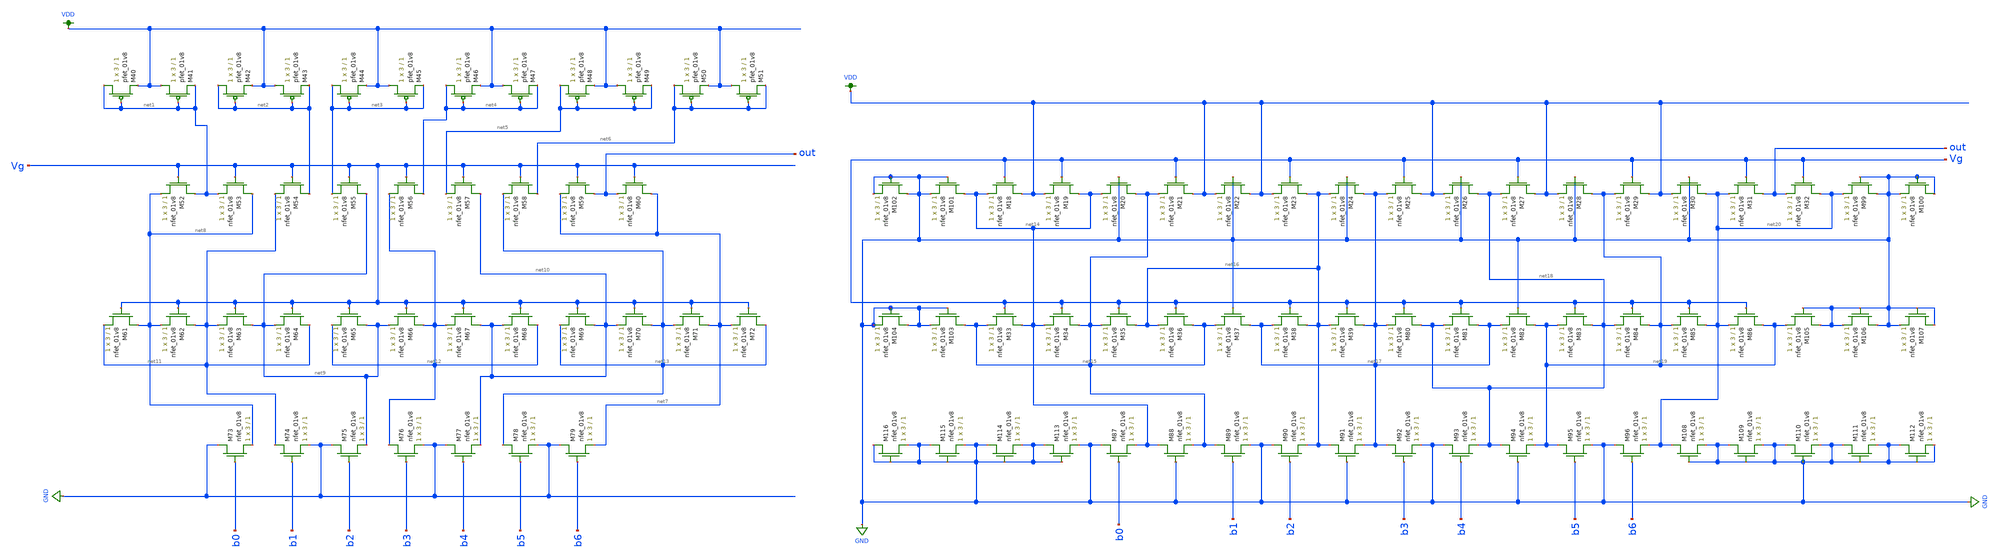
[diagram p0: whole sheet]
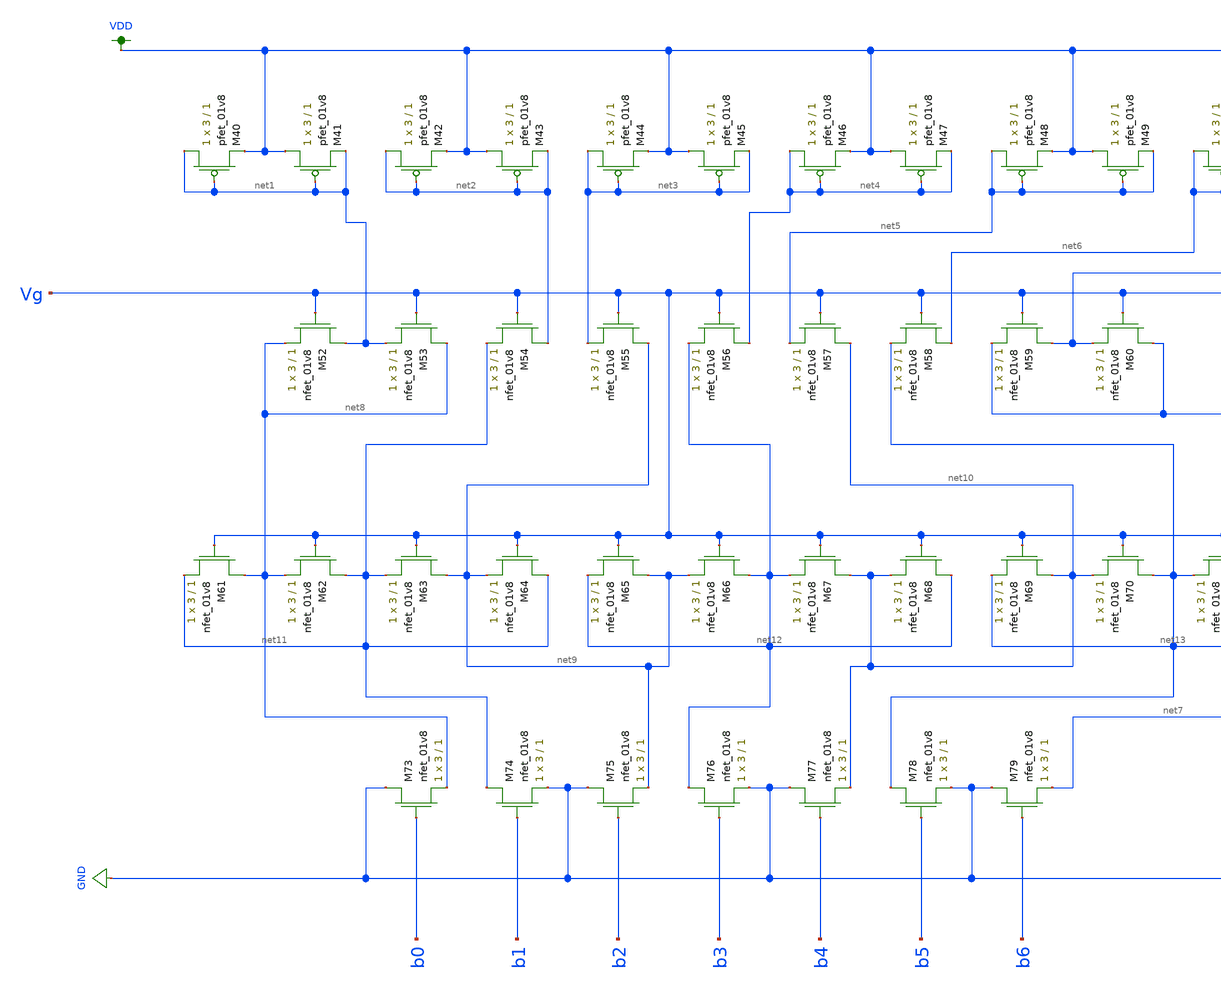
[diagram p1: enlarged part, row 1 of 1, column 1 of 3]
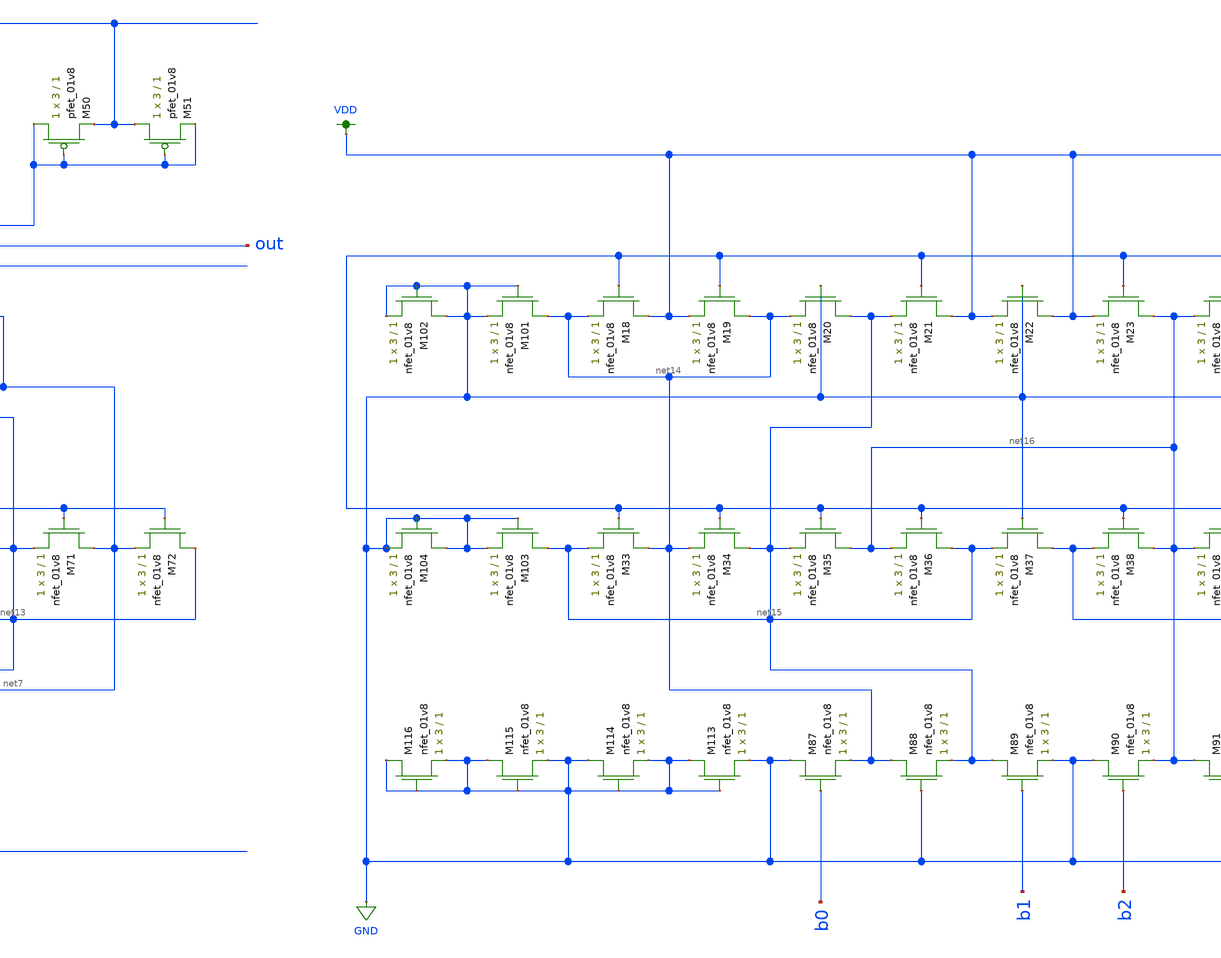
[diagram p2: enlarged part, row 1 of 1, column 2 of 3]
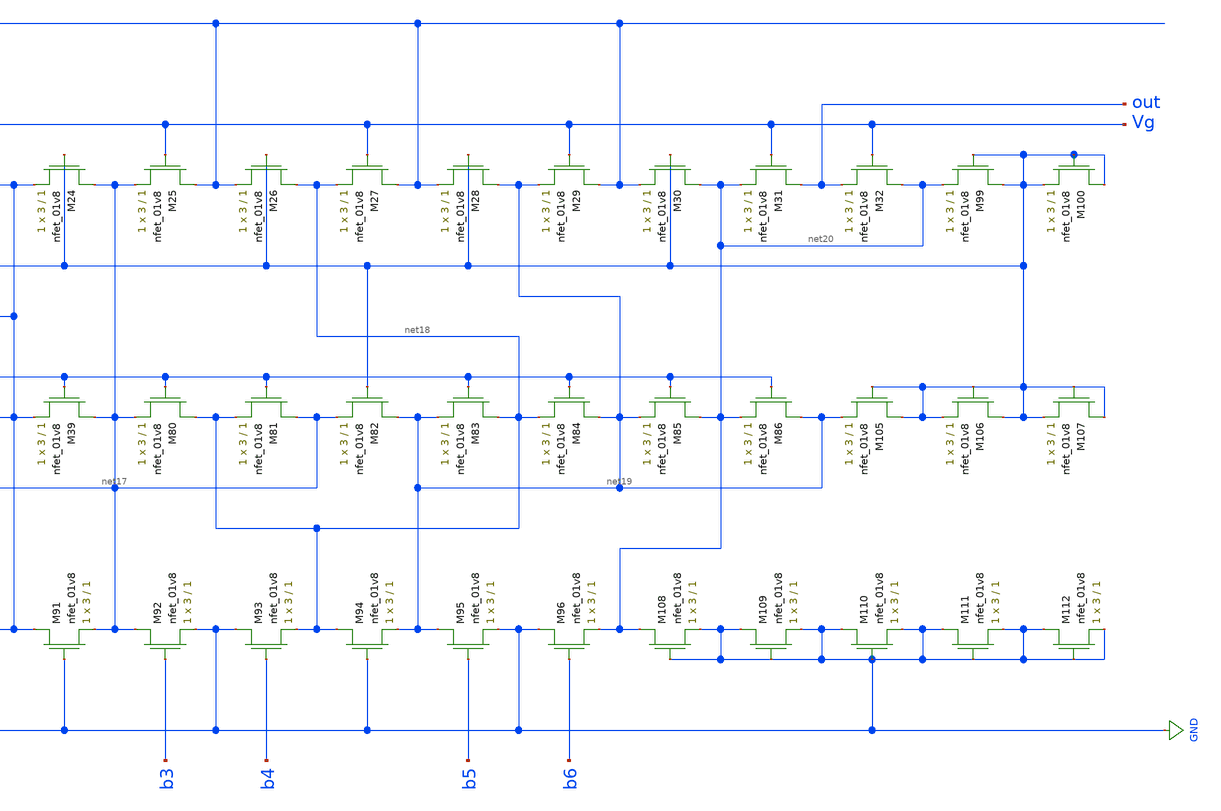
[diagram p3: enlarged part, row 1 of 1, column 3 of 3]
** sch_path: schematic/LDS/old/dac_7_bit_LDS_old.sch
**.subckt dac_7_bit_LDS_old
XM40 net1 net1 VDD VDD sky130_fd_pr__pfet_01v8 L=1 W=3 nf=1 ad='int((nf+1)/2) * W/nf * 0.29' as='int((nf+2)/2) * W/nf * 0.29'
+ pd='2*int((nf+1)/2) * (W/nf + 0.29)' ps='2*int((nf+2)/2) * (W/nf + 0.29)' nrd='0.29 / W' nrs='0.29 / W'
+ sa=0 sb=0 sd=0 mult=1 m=1
XM41 VDD net1 net1 VDD sky130_fd_pr__pfet_01v8 L=1 W=3 nf=1 ad='int((nf+1)/2) * W/nf * 0.29' as='int((nf+2)/2) * W/nf * 0.29'
+ pd='2*int((nf+1)/2) * (W/nf + 0.29)' ps='2*int((nf+2)/2) * (W/nf + 0.29)' nrd='0.29 / W' nrs='0.29 / W'
+ sa=0 sb=0 sd=0 mult=1 m=1
XM42 net2 net2 VDD VDD sky130_fd_pr__pfet_01v8 L=1 W=3 nf=1 ad='int((nf+1)/2) * W/nf * 0.29' as='int((nf+2)/2) * W/nf * 0.29'
+ pd='2*int((nf+1)/2) * (W/nf + 0.29)' ps='2*int((nf+2)/2) * (W/nf + 0.29)' nrd='0.29 / W' nrs='0.29 / W'
+ sa=0 sb=0 sd=0 mult=1 m=1
XM43 VDD net2 net2 VDD sky130_fd_pr__pfet_01v8 L=1 W=3 nf=1 ad='int((nf+1)/2) * W/nf * 0.29' as='int((nf+2)/2) * W/nf * 0.29'
+ pd='2*int((nf+1)/2) * (W/nf + 0.29)' ps='2*int((nf+2)/2) * (W/nf + 0.29)' nrd='0.29 / W' nrs='0.29 / W'
+ sa=0 sb=0 sd=0 mult=1 m=1
XM44 net3 net3 VDD VDD sky130_fd_pr__pfet_01v8 L=1 W=3 nf=1 ad='int((nf+1)/2) * W/nf * 0.29' as='int((nf+2)/2) * W/nf * 0.29'
+ pd='2*int((nf+1)/2) * (W/nf + 0.29)' ps='2*int((nf+2)/2) * (W/nf + 0.29)' nrd='0.29 / W' nrs='0.29 / W'
+ sa=0 sb=0 sd=0 mult=1 m=1
XM45 VDD net3 net3 VDD sky130_fd_pr__pfet_01v8 L=1 W=3 nf=1 ad='int((nf+1)/2) * W/nf * 0.29' as='int((nf+2)/2) * W/nf * 0.29'
+ pd='2*int((nf+1)/2) * (W/nf + 0.29)' ps='2*int((nf+2)/2) * (W/nf + 0.29)' nrd='0.29 / W' nrs='0.29 / W'
+ sa=0 sb=0 sd=0 mult=1 m=1
XM46 net4 net4 VDD VDD sky130_fd_pr__pfet_01v8 L=1 W=3 nf=1 ad='int((nf+1)/2) * W/nf * 0.29' as='int((nf+2)/2) * W/nf * 0.29'
+ pd='2*int((nf+1)/2) * (W/nf + 0.29)' ps='2*int((nf+2)/2) * (W/nf + 0.29)' nrd='0.29 / W' nrs='0.29 / W'
+ sa=0 sb=0 sd=0 mult=1 m=1
XM47 VDD net4 net4 VDD sky130_fd_pr__pfet_01v8 L=1 W=3 nf=1 ad='int((nf+1)/2) * W/nf * 0.29' as='int((nf+2)/2) * W/nf * 0.29'
+ pd='2*int((nf+1)/2) * (W/nf + 0.29)' ps='2*int((nf+2)/2) * (W/nf + 0.29)' nrd='0.29 / W' nrs='0.29 / W'
+ sa=0 sb=0 sd=0 mult=1 m=1
XM48 net5 net5 VDD VDD sky130_fd_pr__pfet_01v8 L=1 W=3 nf=1 ad='int((nf+1)/2) * W/nf * 0.29' as='int((nf+2)/2) * W/nf * 0.29'
+ pd='2*int((nf+1)/2) * (W/nf + 0.29)' ps='2*int((nf+2)/2) * (W/nf + 0.29)' nrd='0.29 / W' nrs='0.29 / W'
+ sa=0 sb=0 sd=0 mult=1 m=1
XM49 VDD net5 net5 VDD sky130_fd_pr__pfet_01v8 L=1 W=3 nf=1 ad='int((nf+1)/2) * W/nf * 0.29' as='int((nf+2)/2) * W/nf * 0.29'
+ pd='2*int((nf+1)/2) * (W/nf + 0.29)' ps='2*int((nf+2)/2) * (W/nf + 0.29)' nrd='0.29 / W' nrs='0.29 / W'
+ sa=0 sb=0 sd=0 mult=1 m=1
XM50 net6 net6 VDD VDD sky130_fd_pr__pfet_01v8 L=1 W=3 nf=1 ad='int((nf+1)/2) * W/nf * 0.29' as='int((nf+2)/2) * W/nf * 0.29'
+ pd='2*int((nf+1)/2) * (W/nf + 0.29)' ps='2*int((nf+2)/2) * (W/nf + 0.29)' nrd='0.29 / W' nrs='0.29 / W'
+ sa=0 sb=0 sd=0 mult=1 m=1
XM51 VDD net6 net6 VDD sky130_fd_pr__pfet_01v8 L=1 W=3 nf=1 ad='int((nf+1)/2) * W/nf * 0.29' as='int((nf+2)/2) * W/nf * 0.29'
+ pd='2*int((nf+1)/2) * (W/nf + 0.29)' ps='2*int((nf+2)/2) * (W/nf + 0.29)' nrd='0.29 / W' nrs='0.29 / W'
+ sa=0 sb=0 sd=0 mult=1 m=1
XM52 net1 Vg net8 GND sky130_fd_pr__nfet_01v8 L=1 W=3 nf=1 ad='int((nf+1)/2) * W/nf * 0.29' as='int((nf+2)/2) * W/nf * 0.29'
+ pd='2*int((nf+1)/2) * (W/nf + 0.29)' ps='2*int((nf+2)/2) * (W/nf + 0.29)' nrd='0.29 / W' nrs='0.29 / W'
+ sa=0 sb=0 sd=0 mult=1 m=1
XM53 net8 Vg net1 GND sky130_fd_pr__nfet_01v8 L=1 W=3 nf=1 ad='int((nf+1)/2) * W/nf * 0.29' as='int((nf+2)/2) * W/nf * 0.29'
+ pd='2*int((nf+1)/2) * (W/nf + 0.29)' ps='2*int((nf+2)/2) * (W/nf + 0.29)' nrd='0.29 / W' nrs='0.29 / W'
+ sa=0 sb=0 sd=0 mult=1 m=1
XM54 net2 Vg net11 GND sky130_fd_pr__nfet_01v8 L=1 W=3 nf=1 ad='int((nf+1)/2) * W/nf * 0.29' as='int((nf+2)/2) * W/nf * 0.29'
+ pd='2*int((nf+1)/2) * (W/nf + 0.29)' ps='2*int((nf+2)/2) * (W/nf + 0.29)' nrd='0.29 / W' nrs='0.29 / W'
+ sa=0 sb=0 sd=0 mult=1 m=1
XM55 net9 Vg net3 GND sky130_fd_pr__nfet_01v8 L=1 W=3 nf=1 ad='int((nf+1)/2) * W/nf * 0.29' as='int((nf+2)/2) * W/nf * 0.29'
+ pd='2*int((nf+1)/2) * (W/nf + 0.29)' ps='2*int((nf+2)/2) * (W/nf + 0.29)' nrd='0.29 / W' nrs='0.29 / W'
+ sa=0 sb=0 sd=0 mult=1 m=1
XM56 net4 Vg net12 GND sky130_fd_pr__nfet_01v8 L=1 W=3 nf=1 ad='int((nf+1)/2) * W/nf * 0.29' as='int((nf+2)/2) * W/nf * 0.29'
+ pd='2*int((nf+1)/2) * (W/nf + 0.29)' ps='2*int((nf+2)/2) * (W/nf + 0.29)' nrd='0.29 / W' nrs='0.29 / W'
+ sa=0 sb=0 sd=0 mult=1 m=1
XM57 net10 Vg net5 GND sky130_fd_pr__nfet_01v8 L=1 W=3 nf=1 ad='int((nf+1)/2) * W/nf * 0.29' as='int((nf+2)/2) * W/nf * 0.29'
+ pd='2*int((nf+1)/2) * (W/nf + 0.29)' ps='2*int((nf+2)/2) * (W/nf + 0.29)' nrd='0.29 / W' nrs='0.29 / W'
+ sa=0 sb=0 sd=0 mult=1 m=1
XM58 net6 Vg net13 GND sky130_fd_pr__nfet_01v8 L=1 W=3 nf=1 ad='int((nf+1)/2) * W/nf * 0.29' as='int((nf+2)/2) * W/nf * 0.29'
+ pd='2*int((nf+1)/2) * (W/nf + 0.29)' ps='2*int((nf+2)/2) * (W/nf + 0.29)' nrd='0.29 / W' nrs='0.29 / W'
+ sa=0 sb=0 sd=0 mult=1 m=1
XM59 out Vg net7 GND sky130_fd_pr__nfet_01v8 L=1 W=3 nf=1 ad='int((nf+1)/2) * W/nf * 0.29' as='int((nf+2)/2) * W/nf * 0.29'
+ pd='2*int((nf+1)/2) * (W/nf + 0.29)' ps='2*int((nf+2)/2) * (W/nf + 0.29)' nrd='0.29 / W' nrs='0.29 / W'
+ sa=0 sb=0 sd=0 mult=1 m=1
XM60 net7 Vg out GND sky130_fd_pr__nfet_01v8 L=1 W=3 nf=1 ad='int((nf+1)/2) * W/nf * 0.29' as='int((nf+2)/2) * W/nf * 0.29'
+ pd='2*int((nf+1)/2) * (W/nf + 0.29)' ps='2*int((nf+2)/2) * (W/nf + 0.29)' nrd='0.29 / W' nrs='0.29 / W'
+ sa=0 sb=0 sd=0 mult=1 m=1
XM61 net8 Vg net11 GND sky130_fd_pr__nfet_01v8 L=1 W=3 nf=1 ad='int((nf+1)/2) * W/nf * 0.29' as='int((nf+2)/2) * W/nf * 0.29'
+ pd='2*int((nf+1)/2) * (W/nf + 0.29)' ps='2*int((nf+2)/2) * (W/nf + 0.29)' nrd='0.29 / W' nrs='0.29 / W'
+ sa=0 sb=0 sd=0 mult=1 m=1
XM62 net11 Vg net8 GND sky130_fd_pr__nfet_01v8 L=1 W=3 nf=1 ad='int((nf+1)/2) * W/nf * 0.29' as='int((nf+2)/2) * W/nf * 0.29'
+ pd='2*int((nf+1)/2) * (W/nf + 0.29)' ps='2*int((nf+2)/2) * (W/nf + 0.29)' nrd='0.29 / W' nrs='0.29 / W'
+ sa=0 sb=0 sd=0 mult=1 m=1
XM63 net9 Vg net11 GND sky130_fd_pr__nfet_01v8 L=1 W=3 nf=1 ad='int((nf+1)/2) * W/nf * 0.29' as='int((nf+2)/2) * W/nf * 0.29'
+ pd='2*int((nf+1)/2) * (W/nf + 0.29)' ps='2*int((nf+2)/2) * (W/nf + 0.29)' nrd='0.29 / W' nrs='0.29 / W'
+ sa=0 sb=0 sd=0 mult=1 m=1
XM64 net11 Vg net9 GND sky130_fd_pr__nfet_01v8 L=1 W=3 nf=1 ad='int((nf+1)/2) * W/nf * 0.29' as='int((nf+2)/2) * W/nf * 0.29'
+ pd='2*int((nf+1)/2) * (W/nf + 0.29)' ps='2*int((nf+2)/2) * (W/nf + 0.29)' nrd='0.29 / W' nrs='0.29 / W'
+ sa=0 sb=0 sd=0 mult=1 m=1
XM65 net9 Vg net12 GND sky130_fd_pr__nfet_01v8 L=1 W=3 nf=1 ad='int((nf+1)/2) * W/nf * 0.29' as='int((nf+2)/2) * W/nf * 0.29'
+ pd='2*int((nf+1)/2) * (W/nf + 0.29)' ps='2*int((nf+2)/2) * (W/nf + 0.29)' nrd='0.29 / W' nrs='0.29 / W'
+ sa=0 sb=0 sd=0 mult=1 m=1
XM66 net12 Vg net9 GND sky130_fd_pr__nfet_01v8 L=1 W=3 nf=1 ad='int((nf+1)/2) * W/nf * 0.29' as='int((nf+2)/2) * W/nf * 0.29'
+ pd='2*int((nf+1)/2) * (W/nf + 0.29)' ps='2*int((nf+2)/2) * (W/nf + 0.29)' nrd='0.29 / W' nrs='0.29 / W'
+ sa=0 sb=0 sd=0 mult=1 m=1
XM67 net10 Vg net12 GND sky130_fd_pr__nfet_01v8 L=1 W=3 nf=1 ad='int((nf+1)/2) * W/nf * 0.29' as='int((nf+2)/2) * W/nf * 0.29'
+ pd='2*int((nf+1)/2) * (W/nf + 0.29)' ps='2*int((nf+2)/2) * (W/nf + 0.29)' nrd='0.29 / W' nrs='0.29 / W'
+ sa=0 sb=0 sd=0 mult=1 m=1
XM68 net12 Vg net10 GND sky130_fd_pr__nfet_01v8 L=1 W=3 nf=1 ad='int((nf+1)/2) * W/nf * 0.29' as='int((nf+2)/2) * W/nf * 0.29'
+ pd='2*int((nf+1)/2) * (W/nf + 0.29)' ps='2*int((nf+2)/2) * (W/nf + 0.29)' nrd='0.29 / W' nrs='0.29 / W'
+ sa=0 sb=0 sd=0 mult=1 m=1
XM69 net10 Vg net13 GND sky130_fd_pr__nfet_01v8 L=1 W=3 nf=1 ad='int((nf+1)/2) * W/nf * 0.29' as='int((nf+2)/2) * W/nf * 0.29'
+ pd='2*int((nf+1)/2) * (W/nf + 0.29)' ps='2*int((nf+2)/2) * (W/nf + 0.29)' nrd='0.29 / W' nrs='0.29 / W'
+ sa=0 sb=0 sd=0 mult=1 m=1
XM70 net13 Vg net10 GND sky130_fd_pr__nfet_01v8 L=1 W=3 nf=1 ad='int((nf+1)/2) * W/nf * 0.29' as='int((nf+2)/2) * W/nf * 0.29'
+ pd='2*int((nf+1)/2) * (W/nf + 0.29)' ps='2*int((nf+2)/2) * (W/nf + 0.29)' nrd='0.29 / W' nrs='0.29 / W'
+ sa=0 sb=0 sd=0 mult=1 m=1
XM71 net7 Vg net13 GND sky130_fd_pr__nfet_01v8 L=1 W=3 nf=1 ad='int((nf+1)/2) * W/nf * 0.29' as='int((nf+2)/2) * W/nf * 0.29'
+ pd='2*int((nf+1)/2) * (W/nf + 0.29)' ps='2*int((nf+2)/2) * (W/nf + 0.29)' nrd='0.29 / W' nrs='0.29 / W'
+ sa=0 sb=0 sd=0 mult=1 m=1
XM72 net13 Vg net7 GND sky130_fd_pr__nfet_01v8 L=1 W=3 nf=1 ad='int((nf+1)/2) * W/nf * 0.29' as='int((nf+2)/2) * W/nf * 0.29'
+ pd='2*int((nf+1)/2) * (W/nf + 0.29)' ps='2*int((nf+2)/2) * (W/nf + 0.29)' nrd='0.29 / W' nrs='0.29 / W'
+ sa=0 sb=0 sd=0 mult=1 m=1
XM73 GND b0 net8 GND sky130_fd_pr__nfet_01v8 L=1 W=3 nf=1 ad='int((nf+1)/2) * W/nf * 0.29' as='int((nf+2)/2) * W/nf * 0.29'
+ pd='2*int((nf+1)/2) * (W/nf + 0.29)' ps='2*int((nf+2)/2) * (W/nf + 0.29)' nrd='0.29 / W' nrs='0.29 / W'
+ sa=0 sb=0 sd=0 mult=1 m=1
XM74 net11 b1 GND GND sky130_fd_pr__nfet_01v8 L=1 W=3 nf=1 ad='int((nf+1)/2) * W/nf * 0.29' as='int((nf+2)/2) * W/nf * 0.29'
+ pd='2*int((nf+1)/2) * (W/nf + 0.29)' ps='2*int((nf+2)/2) * (W/nf + 0.29)' nrd='0.29 / W' nrs='0.29 / W'
+ sa=0 sb=0 sd=0 mult=1 m=1
XM75 GND b2 net9 GND sky130_fd_pr__nfet_01v8 L=1 W=3 nf=1 ad='int((nf+1)/2) * W/nf * 0.29' as='int((nf+2)/2) * W/nf * 0.29'
+ pd='2*int((nf+1)/2) * (W/nf + 0.29)' ps='2*int((nf+2)/2) * (W/nf + 0.29)' nrd='0.29 / W' nrs='0.29 / W'
+ sa=0 sb=0 sd=0 mult=1 m=1
XM76 net12 b3 GND GND sky130_fd_pr__nfet_01v8 L=1 W=3 nf=1 ad='int((nf+1)/2) * W/nf * 0.29' as='int((nf+2)/2) * W/nf * 0.29'
+ pd='2*int((nf+1)/2) * (W/nf + 0.29)' ps='2*int((nf+2)/2) * (W/nf + 0.29)' nrd='0.29 / W' nrs='0.29 / W'
+ sa=0 sb=0 sd=0 mult=1 m=1
XM77 GND b4 net10 GND sky130_fd_pr__nfet_01v8 L=1 W=3 nf=1 ad='int((nf+1)/2) * W/nf * 0.29' as='int((nf+2)/2) * W/nf * 0.29'
+ pd='2*int((nf+1)/2) * (W/nf + 0.29)' ps='2*int((nf+2)/2) * (W/nf + 0.29)' nrd='0.29 / W' nrs='0.29 / W'
+ sa=0 sb=0 sd=0 mult=1 m=1
XM78 net13 b5 GND GND sky130_fd_pr__nfet_01v8 L=1 W=3 nf=1 ad='int((nf+1)/2) * W/nf * 0.29' as='int((nf+2)/2) * W/nf * 0.29'
+ pd='2*int((nf+1)/2) * (W/nf + 0.29)' ps='2*int((nf+2)/2) * (W/nf + 0.29)' nrd='0.29 / W' nrs='0.29 / W'
+ sa=0 sb=0 sd=0 mult=1 m=1
XM79 GND b6 net7 GND sky130_fd_pr__nfet_01v8 L=1 W=3 nf=1 ad='int((nf+1)/2) * W/nf * 0.29' as='int((nf+2)/2) * W/nf * 0.29'
+ pd='2*int((nf+1)/2) * (W/nf + 0.29)' ps='2*int((nf+2)/2) * (W/nf + 0.29)' nrd='0.29 / W' nrs='0.29 / W'
+ sa=0 sb=0 sd=0 mult=1 m=1
XM18 VDD Vg net14 GND sky130_fd_pr__nfet_01v8 L=1 W=3 nf=1 ad='int((nf+1)/2) * W/nf * 0.29' as='int((nf+2)/2) * W/nf * 0.29'
+ pd='2*int((nf+1)/2) * (W/nf + 0.29)' ps='2*int((nf+2)/2) * (W/nf + 0.29)' nrd='0.29 / W' nrs='0.29 / W'
+ sa=0 sb=0 sd=0 mult=1 m=1
XM19 net14 Vg VDD GND sky130_fd_pr__nfet_01v8 L=1 W=3 nf=1 ad='int((nf+1)/2) * W/nf * 0.29' as='int((nf+2)/2) * W/nf * 0.29'
+ pd='2*int((nf+1)/2) * (W/nf + 0.29)' ps='2*int((nf+2)/2) * (W/nf + 0.29)' nrd='0.29 / W' nrs='0.29 / W'
+ sa=0 sb=0 sd=0 mult=1 m=1
XM20 net15 GND net14 GND sky130_fd_pr__nfet_01v8 L=1 W=3 nf=1 ad='int((nf+1)/2) * W/nf * 0.29' as='int((nf+2)/2) * W/nf * 0.29'
+ pd='2*int((nf+1)/2) * (W/nf + 0.29)' ps='2*int((nf+2)/2) * (W/nf + 0.29)' nrd='0.29 / W' nrs='0.29 / W'
+ sa=0 sb=0 sd=0 mult=1 m=1
XM21 VDD Vg net15 GND sky130_fd_pr__nfet_01v8 L=1 W=3 nf=1 ad='int((nf+1)/2) * W/nf * 0.29' as='int((nf+2)/2) * W/nf * 0.29'
+ pd='2*int((nf+1)/2) * (W/nf + 0.29)' ps='2*int((nf+2)/2) * (W/nf + 0.29)' nrd='0.29 / W' nrs='0.29 / W'
+ sa=0 sb=0 sd=0 mult=1 m=1
XM22 VDD GND VDD GND sky130_fd_pr__nfet_01v8 L=1 W=3 nf=1 ad='int((nf+1)/2) * W/nf * 0.29' as='int((nf+2)/2) * W/nf * 0.29'
+ pd='2*int((nf+1)/2) * (W/nf + 0.29)' ps='2*int((nf+2)/2) * (W/nf + 0.29)' nrd='0.29 / W' nrs='0.29 / W'
+ sa=0 sb=0 sd=0 mult=1 m=1
XM23 net16 Vg VDD GND sky130_fd_pr__nfet_01v8 L=1 W=3 nf=1 ad='int((nf+1)/2) * W/nf * 0.29' as='int((nf+2)/2) * W/nf * 0.29'
+ pd='2*int((nf+1)/2) * (W/nf + 0.29)' ps='2*int((nf+2)/2) * (W/nf + 0.29)' nrd='0.29 / W' nrs='0.29 / W'
+ sa=0 sb=0 sd=0 mult=1 m=1
XM24 net17 GND net16 GND sky130_fd_pr__nfet_01v8 L=1 W=3 nf=1 ad='int((nf+1)/2) * W/nf * 0.29' as='int((nf+2)/2) * W/nf * 0.29'
+ pd='2*int((nf+1)/2) * (W/nf + 0.29)' ps='2*int((nf+2)/2) * (W/nf + 0.29)' nrd='0.29 / W' nrs='0.29 / W'
+ sa=0 sb=0 sd=0 mult=1 m=1
XM25 VDD Vg net17 GND sky130_fd_pr__nfet_01v8 L=1 W=3 nf=1 ad='int((nf+1)/2) * W/nf * 0.29' as='int((nf+2)/2) * W/nf * 0.29'
+ pd='2*int((nf+1)/2) * (W/nf + 0.29)' ps='2*int((nf+2)/2) * (W/nf + 0.29)' nrd='0.29 / W' nrs='0.29 / W'
+ sa=0 sb=0 sd=0 mult=1 m=1
XM26 net18 GND VDD GND sky130_fd_pr__nfet_01v8 L=1 W=3 nf=1 ad='int((nf+1)/2) * W/nf * 0.29' as='int((nf+2)/2) * W/nf * 0.29'
+ pd='2*int((nf+1)/2) * (W/nf + 0.29)' ps='2*int((nf+2)/2) * (W/nf + 0.29)' nrd='0.29 / W' nrs='0.29 / W'
+ sa=0 sb=0 sd=0 mult=1 m=1
XM27 VDD Vg net18 GND sky130_fd_pr__nfet_01v8 L=1 W=3 nf=1 ad='int((nf+1)/2) * W/nf * 0.29' as='int((nf+2)/2) * W/nf * 0.29'
+ pd='2*int((nf+1)/2) * (W/nf + 0.29)' ps='2*int((nf+2)/2) * (W/nf + 0.29)' nrd='0.29 / W' nrs='0.29 / W'
+ sa=0 sb=0 sd=0 mult=1 m=1
XM28 net19 GND VDD GND sky130_fd_pr__nfet_01v8 L=1 W=3 nf=1 ad='int((nf+1)/2) * W/nf * 0.29' as='int((nf+2)/2) * W/nf * 0.29'
+ pd='2*int((nf+1)/2) * (W/nf + 0.29)' ps='2*int((nf+2)/2) * (W/nf + 0.29)' nrd='0.29 / W' nrs='0.29 / W'
+ sa=0 sb=0 sd=0 mult=1 m=1
XM29 VDD Vg net19 GND sky130_fd_pr__nfet_01v8 L=1 W=3 nf=1 ad='int((nf+1)/2) * W/nf * 0.29' as='int((nf+2)/2) * W/nf * 0.29'
+ pd='2*int((nf+1)/2) * (W/nf + 0.29)' ps='2*int((nf+2)/2) * (W/nf + 0.29)' nrd='0.29 / W' nrs='0.29 / W'
+ sa=0 sb=0 sd=0 mult=1 m=1
XM30 net20 GND VDD GND sky130_fd_pr__nfet_01v8 L=1 W=3 nf=1 ad='int((nf+1)/2) * W/nf * 0.29' as='int((nf+2)/2) * W/nf * 0.29'
+ pd='2*int((nf+1)/2) * (W/nf + 0.29)' ps='2*int((nf+2)/2) * (W/nf + 0.29)' nrd='0.29 / W' nrs='0.29 / W'
+ sa=0 sb=0 sd=0 mult=1 m=1
XM31 out Vg net20 GND sky130_fd_pr__nfet_01v8 L=1 W=3 nf=1 ad='int((nf+1)/2) * W/nf * 0.29' as='int((nf+2)/2) * W/nf * 0.29'
+ pd='2*int((nf+1)/2) * (W/nf + 0.29)' ps='2*int((nf+2)/2) * (W/nf + 0.29)' nrd='0.29 / W' nrs='0.29 / W'
+ sa=0 sb=0 sd=0 mult=1 m=1
XM32 net20 Vg out GND sky130_fd_pr__nfet_01v8 L=1 W=3 nf=1 ad='int((nf+1)/2) * W/nf * 0.29' as='int((nf+2)/2) * W/nf * 0.29'
+ pd='2*int((nf+1)/2) * (W/nf + 0.29)' ps='2*int((nf+2)/2) * (W/nf + 0.29)' nrd='0.29 / W' nrs='0.29 / W'
+ sa=0 sb=0 sd=0 mult=1 m=1
XM33 net14 Vg net15 GND sky130_fd_pr__nfet_01v8 L=1 W=3 nf=1 ad='int((nf+1)/2) * W/nf * 0.29' as='int((nf+2)/2) * W/nf * 0.29'
+ pd='2*int((nf+1)/2) * (W/nf + 0.29)' ps='2*int((nf+2)/2) * (W/nf + 0.29)' nrd='0.29 / W' nrs='0.29 / W'
+ sa=0 sb=0 sd=0 mult=1 m=1
XM34 net15 Vg net14 GND sky130_fd_pr__nfet_01v8 L=1 W=3 nf=1 ad='int((nf+1)/2) * W/nf * 0.29' as='int((nf+2)/2) * W/nf * 0.29'
+ pd='2*int((nf+1)/2) * (W/nf + 0.29)' ps='2*int((nf+2)/2) * (W/nf + 0.29)' nrd='0.29 / W' nrs='0.29 / W'
+ sa=0 sb=0 sd=0 mult=1 m=1
XM35 net16 Vg net15 GND sky130_fd_pr__nfet_01v8 L=1 W=3 nf=1 ad='int((nf+1)/2) * W/nf * 0.29' as='int((nf+2)/2) * W/nf * 0.29'
+ pd='2*int((nf+1)/2) * (W/nf + 0.29)' ps='2*int((nf+2)/2) * (W/nf + 0.29)' nrd='0.29 / W' nrs='0.29 / W'
+ sa=0 sb=0 sd=0 mult=1 m=1
XM36 net15 Vg net16 GND sky130_fd_pr__nfet_01v8 L=1 W=3 nf=1 ad='int((nf+1)/2) * W/nf * 0.29' as='int((nf+2)/2) * W/nf * 0.29'
+ pd='2*int((nf+1)/2) * (W/nf + 0.29)' ps='2*int((nf+2)/2) * (W/nf + 0.29)' nrd='0.29 / W' nrs='0.29 / W'
+ sa=0 sb=0 sd=0 mult=1 m=1
XM37 net17 GND net15 GND sky130_fd_pr__nfet_01v8 L=1 W=3 nf=1 ad='int((nf+1)/2) * W/nf * 0.29' as='int((nf+2)/2) * W/nf * 0.29'
+ pd='2*int((nf+1)/2) * (W/nf + 0.29)' ps='2*int((nf+2)/2) * (W/nf + 0.29)' nrd='0.29 / W' nrs='0.29 / W'
+ sa=0 sb=0 sd=0 mult=1 m=1
XM38 net16 Vg net17 GND sky130_fd_pr__nfet_01v8 L=1 W=3 nf=1 ad='int((nf+1)/2) * W/nf * 0.29' as='int((nf+2)/2) * W/nf * 0.29'
+ pd='2*int((nf+1)/2) * (W/nf + 0.29)' ps='2*int((nf+2)/2) * (W/nf + 0.29)' nrd='0.29 / W' nrs='0.29 / W'
+ sa=0 sb=0 sd=0 mult=1 m=1
XM39 net17 Vg net16 GND sky130_fd_pr__nfet_01v8 L=1 W=3 nf=1 ad='int((nf+1)/2) * W/nf * 0.29' as='int((nf+2)/2) * W/nf * 0.29'
+ pd='2*int((nf+1)/2) * (W/nf + 0.29)' ps='2*int((nf+2)/2) * (W/nf + 0.29)' nrd='0.29 / W' nrs='0.29 / W'
+ sa=0 sb=0 sd=0 mult=1 m=1
XM80 net18 Vg net17 GND sky130_fd_pr__nfet_01v8 L=1 W=3 nf=1 ad='int((nf+1)/2) * W/nf * 0.29' as='int((nf+2)/2) * W/nf * 0.29'
+ pd='2*int((nf+1)/2) * (W/nf + 0.29)' ps='2*int((nf+2)/2) * (W/nf + 0.29)' nrd='0.29 / W' nrs='0.29 / W'
+ sa=0 sb=0 sd=0 mult=1 m=1
XM81 net17 Vg net18 GND sky130_fd_pr__nfet_01v8 L=1 W=3 nf=1 ad='int((nf+1)/2) * W/nf * 0.29' as='int((nf+2)/2) * W/nf * 0.29'
+ pd='2*int((nf+1)/2) * (W/nf + 0.29)' ps='2*int((nf+2)/2) * (W/nf + 0.29)' nrd='0.29 / W' nrs='0.29 / W'
+ sa=0 sb=0 sd=0 mult=1 m=1
XM82 net19 GND net17 GND sky130_fd_pr__nfet_01v8 L=1 W=3 nf=1 ad='int((nf+1)/2) * W/nf * 0.29' as='int((nf+2)/2) * W/nf * 0.29'
+ pd='2*int((nf+1)/2) * (W/nf + 0.29)' ps='2*int((nf+2)/2) * (W/nf + 0.29)' nrd='0.29 / W' nrs='0.29 / W'
+ sa=0 sb=0 sd=0 mult=1 m=1
XM83 net18 Vg net19 GND sky130_fd_pr__nfet_01v8 L=1 W=3 nf=1 ad='int((nf+1)/2) * W/nf * 0.29' as='int((nf+2)/2) * W/nf * 0.29'
+ pd='2*int((nf+1)/2) * (W/nf + 0.29)' ps='2*int((nf+2)/2) * (W/nf + 0.29)' nrd='0.29 / W' nrs='0.29 / W'
+ sa=0 sb=0 sd=0 mult=1 m=1
XM84 net19 Vg net18 GND sky130_fd_pr__nfet_01v8 L=1 W=3 nf=1 ad='int((nf+1)/2) * W/nf * 0.29' as='int((nf+2)/2) * W/nf * 0.29'
+ pd='2*int((nf+1)/2) * (W/nf + 0.29)' ps='2*int((nf+2)/2) * (W/nf + 0.29)' nrd='0.29 / W' nrs='0.29 / W'
+ sa=0 sb=0 sd=0 mult=1 m=1
XM85 net20 Vg net19 GND sky130_fd_pr__nfet_01v8 L=1 W=3 nf=1 ad='int((nf+1)/2) * W/nf * 0.29' as='int((nf+2)/2) * W/nf * 0.29'
+ pd='2*int((nf+1)/2) * (W/nf + 0.29)' ps='2*int((nf+2)/2) * (W/nf + 0.29)' nrd='0.29 / W' nrs='0.29 / W'
+ sa=0 sb=0 sd=0 mult=1 m=1
XM86 net19 Vg net20 GND sky130_fd_pr__nfet_01v8 L=1 W=3 nf=1 ad='int((nf+1)/2) * W/nf * 0.29' as='int((nf+2)/2) * W/nf * 0.29'
+ pd='2*int((nf+1)/2) * (W/nf + 0.29)' ps='2*int((nf+2)/2) * (W/nf + 0.29)' nrd='0.29 / W' nrs='0.29 / W'
+ sa=0 sb=0 sd=0 mult=1 m=1
XM87 GND b0 net14 GND sky130_fd_pr__nfet_01v8 L=1 W=3 nf=1 ad='int((nf+1)/2) * W/nf * 0.29' as='int((nf+2)/2) * W/nf * 0.29'
+ pd='2*int((nf+1)/2) * (W/nf + 0.29)' ps='2*int((nf+2)/2) * (W/nf + 0.29)' nrd='0.29 / W' nrs='0.29 / W'
+ sa=0 sb=0 sd=0 mult=1 m=1
XM88 net14 GND net15 GND sky130_fd_pr__nfet_01v8 L=1 W=3 nf=1 ad='int((nf+1)/2) * W/nf * 0.29' as='int((nf+2)/2) * W/nf * 0.29'
+ pd='2*int((nf+1)/2) * (W/nf + 0.29)' ps='2*int((nf+2)/2) * (W/nf + 0.29)' nrd='0.29 / W' nrs='0.29 / W'
+ sa=0 sb=0 sd=0 mult=1 m=1
XM89 net15 b1 GND GND sky130_fd_pr__nfet_01v8 L=1 W=3 nf=1 ad='int((nf+1)/2) * W/nf * 0.29' as='int((nf+2)/2) * W/nf * 0.29'
+ pd='2*int((nf+1)/2) * (W/nf + 0.29)' ps='2*int((nf+2)/2) * (W/nf + 0.29)' nrd='0.29 / W' nrs='0.29 / W'
+ sa=0 sb=0 sd=0 mult=1 m=1
XM90 GND b2 net16 GND sky130_fd_pr__nfet_01v8 L=1 W=3 nf=1 ad='int((nf+1)/2) * W/nf * 0.29' as='int((nf+2)/2) * W/nf * 0.29'
+ pd='2*int((nf+1)/2) * (W/nf + 0.29)' ps='2*int((nf+2)/2) * (W/nf + 0.29)' nrd='0.29 / W' nrs='0.29 / W'
+ sa=0 sb=0 sd=0 mult=1 m=1
XM91 net16 GND net17 GND sky130_fd_pr__nfet_01v8 L=1 W=3 nf=1 ad='int((nf+1)/2) * W/nf * 0.29' as='int((nf+2)/2) * W/nf * 0.29'
+ pd='2*int((nf+1)/2) * (W/nf + 0.29)' ps='2*int((nf+2)/2) * (W/nf + 0.29)' nrd='0.29 / W' nrs='0.29 / W'
+ sa=0 sb=0 sd=0 mult=1 m=1
XM92 net17 b3 GND GND sky130_fd_pr__nfet_01v8 L=1 W=3 nf=1 ad='int((nf+1)/2) * W/nf * 0.29' as='int((nf+2)/2) * W/nf * 0.29'
+ pd='2*int((nf+1)/2) * (W/nf + 0.29)' ps='2*int((nf+2)/2) * (W/nf + 0.29)' nrd='0.29 / W' nrs='0.29 / W'
+ sa=0 sb=0 sd=0 mult=1 m=1
XM93 GND b4 net18 GND sky130_fd_pr__nfet_01v8 L=1 W=3 nf=1 ad='int((nf+1)/2) * W/nf * 0.29' as='int((nf+2)/2) * W/nf * 0.29'
+ pd='2*int((nf+1)/2) * (W/nf + 0.29)' ps='2*int((nf+2)/2) * (W/nf + 0.29)' nrd='0.29 / W' nrs='0.29 / W'
+ sa=0 sb=0 sd=0 mult=1 m=1
XM94 net18 GND net19 GND sky130_fd_pr__nfet_01v8 L=1 W=3 nf=1 ad='int((nf+1)/2) * W/nf * 0.29' as='int((nf+2)/2) * W/nf * 0.29'
+ pd='2*int((nf+1)/2) * (W/nf + 0.29)' ps='2*int((nf+2)/2) * (W/nf + 0.29)' nrd='0.29 / W' nrs='0.29 / W'
+ sa=0 sb=0 sd=0 mult=1 m=1
XM95 net19 b5 GND GND sky130_fd_pr__nfet_01v8 L=1 W=3 nf=1 ad='int((nf+1)/2) * W/nf * 0.29' as='int((nf+2)/2) * W/nf * 0.29'
+ pd='2*int((nf+1)/2) * (W/nf + 0.29)' ps='2*int((nf+2)/2) * (W/nf + 0.29)' nrd='0.29 / W' nrs='0.29 / W'
+ sa=0 sb=0 sd=0 mult=1 m=1
XM96 GND b6 net20 GND sky130_fd_pr__nfet_01v8 L=1 W=3 nf=1 ad='int((nf+1)/2) * W/nf * 0.29' as='int((nf+2)/2) * W/nf * 0.29'
+ pd='2*int((nf+1)/2) * (W/nf + 0.29)' ps='2*int((nf+2)/2) * (W/nf + 0.29)' nrd='0.29 / W' nrs='0.29 / W'
+ sa=0 sb=0 sd=0 mult=1 m=1
XM99 GND GND net20 GND sky130_fd_pr__nfet_01v8 L=1 W=3 nf=1 ad='int((nf+1)/2) * W/nf * 0.29' as='int((nf+2)/2) * W/nf * 0.29'
+ pd='2*int((nf+1)/2) * (W/nf + 0.29)' ps='2*int((nf+2)/2) * (W/nf + 0.29)' nrd='0.29 / W' nrs='0.29 / W'
+ sa=0 sb=0 sd=0 mult=1 m=1
XM100 GND GND GND GND sky130_fd_pr__nfet_01v8 L=1 W=3 nf=1 ad='int((nf+1)/2) * W/nf * 0.29' as='int((nf+2)/2) * W/nf * 0.29'
+ pd='2*int((nf+1)/2) * (W/nf + 0.29)' ps='2*int((nf+2)/2) * (W/nf + 0.29)' nrd='0.29 / W' nrs='0.29 / W'
+ sa=0 sb=0 sd=0 mult=1 m=1
XM101 net14 GND GND GND sky130_fd_pr__nfet_01v8 L=1 W=3 nf=1 ad='int((nf+1)/2) * W/nf * 0.29' as='int((nf+2)/2) * W/nf * 0.29'
+ pd='2*int((nf+1)/2) * (W/nf + 0.29)' ps='2*int((nf+2)/2) * (W/nf + 0.29)' nrd='0.29 / W' nrs='0.29 / W'
+ sa=0 sb=0 sd=0 mult=1 m=1
XM102 GND GND GND GND sky130_fd_pr__nfet_01v8 L=1 W=3 nf=1 ad='int((nf+1)/2) * W/nf * 0.29' as='int((nf+2)/2) * W/nf * 0.29'
+ pd='2*int((nf+1)/2) * (W/nf + 0.29)' ps='2*int((nf+2)/2) * (W/nf + 0.29)' nrd='0.29 / W' nrs='0.29 / W'
+ sa=0 sb=0 sd=0 mult=1 m=1
XM103 net15 GND GND GND sky130_fd_pr__nfet_01v8 L=1 W=3 nf=1 ad='int((nf+1)/2) * W/nf * 0.29' as='int((nf+2)/2) * W/nf * 0.29'
+ pd='2*int((nf+1)/2) * (W/nf + 0.29)' ps='2*int((nf+2)/2) * (W/nf + 0.29)' nrd='0.29 / W' nrs='0.29 / W'
+ sa=0 sb=0 sd=0 mult=1 m=1
XM104 GND GND GND GND sky130_fd_pr__nfet_01v8 L=1 W=3 nf=1 ad='int((nf+1)/2) * W/nf * 0.29' as='int((nf+2)/2) * W/nf * 0.29'
+ pd='2*int((nf+1)/2) * (W/nf + 0.29)' ps='2*int((nf+2)/2) * (W/nf + 0.29)' nrd='0.29 / W' nrs='0.29 / W'
+ sa=0 sb=0 sd=0 mult=1 m=1
XM105 GND GND net19 GND sky130_fd_pr__nfet_01v8 L=1 W=3 nf=1 ad='int((nf+1)/2) * W/nf * 0.29' as='int((nf+2)/2) * W/nf * 0.29'
+ pd='2*int((nf+1)/2) * (W/nf + 0.29)' ps='2*int((nf+2)/2) * (W/nf + 0.29)' nrd='0.29 / W' nrs='0.29 / W'
+ sa=0 sb=0 sd=0 mult=1 m=1
XM106 GND GND GND GND sky130_fd_pr__nfet_01v8 L=1 W=3 nf=1 ad='int((nf+1)/2) * W/nf * 0.29' as='int((nf+2)/2) * W/nf * 0.29'
+ pd='2*int((nf+1)/2) * (W/nf + 0.29)' ps='2*int((nf+2)/2) * (W/nf + 0.29)' nrd='0.29 / W' nrs='0.29 / W'
+ sa=0 sb=0 sd=0 mult=1 m=1
XM107 GND GND GND GND sky130_fd_pr__nfet_01v8 L=1 W=3 nf=1 ad='int((nf+1)/2) * W/nf * 0.29' as='int((nf+2)/2) * W/nf * 0.29'
+ pd='2*int((nf+1)/2) * (W/nf + 0.29)' ps='2*int((nf+2)/2) * (W/nf + 0.29)' nrd='0.29 / W' nrs='0.29 / W'
+ sa=0 sb=0 sd=0 mult=1 m=1
XM108 net20 GND GND GND sky130_fd_pr__nfet_01v8 L=1 W=3 nf=1 ad='int((nf+1)/2) * W/nf * 0.29' as='int((nf+2)/2) * W/nf * 0.29'
+ pd='2*int((nf+1)/2) * (W/nf + 0.29)' ps='2*int((nf+2)/2) * (W/nf + 0.29)' nrd='0.29 / W' nrs='0.29 / W'
+ sa=0 sb=0 sd=0 mult=1 m=1
XM109 GND GND GND GND sky130_fd_pr__nfet_01v8 L=1 W=3 nf=1 ad='int((nf+1)/2) * W/nf * 0.29' as='int((nf+2)/2) * W/nf * 0.29'
+ pd='2*int((nf+1)/2) * (W/nf + 0.29)' ps='2*int((nf+2)/2) * (W/nf + 0.29)' nrd='0.29 / W' nrs='0.29 / W'
+ sa=0 sb=0 sd=0 mult=1 m=1
XM110 GND GND GND GND sky130_fd_pr__nfet_01v8 L=1 W=3 nf=1 ad='int((nf+1)/2) * W/nf * 0.29' as='int((nf+2)/2) * W/nf * 0.29'
+ pd='2*int((nf+1)/2) * (W/nf + 0.29)' ps='2*int((nf+2)/2) * (W/nf + 0.29)' nrd='0.29 / W' nrs='0.29 / W'
+ sa=0 sb=0 sd=0 mult=1 m=1
XM111 GND GND GND GND sky130_fd_pr__nfet_01v8 L=1 W=3 nf=1 ad='int((nf+1)/2) * W/nf * 0.29' as='int((nf+2)/2) * W/nf * 0.29'
+ pd='2*int((nf+1)/2) * (W/nf + 0.29)' ps='2*int((nf+2)/2) * (W/nf + 0.29)' nrd='0.29 / W' nrs='0.29 / W'
+ sa=0 sb=0 sd=0 mult=1 m=1
XM112 GND GND GND GND sky130_fd_pr__nfet_01v8 L=1 W=3 nf=1 ad='int((nf+1)/2) * W/nf * 0.29' as='int((nf+2)/2) * W/nf * 0.29'
+ pd='2*int((nf+1)/2) * (W/nf + 0.29)' ps='2*int((nf+2)/2) * (W/nf + 0.29)' nrd='0.29 / W' nrs='0.29 / W'
+ sa=0 sb=0 sd=0 mult=1 m=1
XM113 GND GND GND GND sky130_fd_pr__nfet_01v8 L=1 W=3 nf=1 ad='int((nf+1)/2) * W/nf * 0.29' as='int((nf+2)/2) * W/nf * 0.29'
+ pd='2*int((nf+1)/2) * (W/nf + 0.29)' ps='2*int((nf+2)/2) * (W/nf + 0.29)' nrd='0.29 / W' nrs='0.29 / W'
+ sa=0 sb=0 sd=0 mult=1 m=1
XM114 GND GND GND GND sky130_fd_pr__nfet_01v8 L=1 W=3 nf=1 ad='int((nf+1)/2) * W/nf * 0.29' as='int((nf+2)/2) * W/nf * 0.29'
+ pd='2*int((nf+1)/2) * (W/nf + 0.29)' ps='2*int((nf+2)/2) * (W/nf + 0.29)' nrd='0.29 / W' nrs='0.29 / W'
+ sa=0 sb=0 sd=0 mult=1 m=1
XM115 GND GND GND GND sky130_fd_pr__nfet_01v8 L=1 W=3 nf=1 ad='int((nf+1)/2) * W/nf * 0.29' as='int((nf+2)/2) * W/nf * 0.29'
+ pd='2*int((nf+1)/2) * (W/nf + 0.29)' ps='2*int((nf+2)/2) * (W/nf + 0.29)' nrd='0.29 / W' nrs='0.29 / W'
+ sa=0 sb=0 sd=0 mult=1 m=1
XM116 GND GND GND GND sky130_fd_pr__nfet_01v8 L=1 W=3 nf=1 ad='int((nf+1)/2) * W/nf * 0.29' as='int((nf+2)/2) * W/nf * 0.29'
+ pd='2*int((nf+1)/2) * (W/nf + 0.29)' ps='2*int((nf+2)/2) * (W/nf + 0.29)' nrd='0.29 / W' nrs='0.29 / W'
+ sa=0 sb=0 sd=0 mult=1 m=1
**.ends
.GLOBAL GND
.GLOBAL VDD
.end
